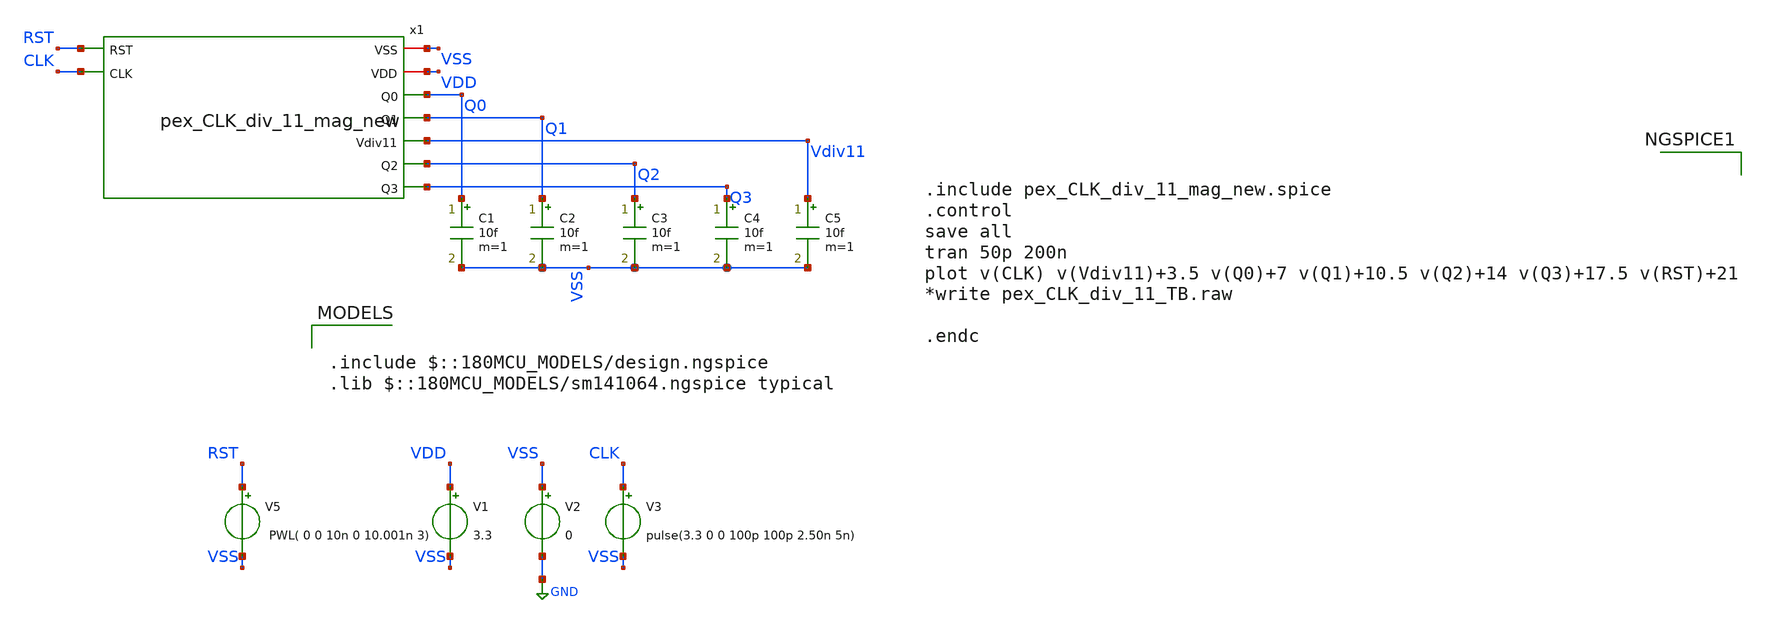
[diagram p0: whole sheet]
** sch_path: Clock_Generator_PAKISTAN_02/xschem/pex_CLK_div_11_TB.sch
**.subckt pex_CLK_div_11_TB
V1 VDD VSS 3.3
V2 VSS GND 0
V3 CLK VSS pulse(3.3 0 0 100p 100p 2.50n 5n)
C1 Q0 VSS 10f m=1
C2 Q1 VSS 10f m=1
C3 Q2 VSS 10f m=1
C4 Q3 VSS 10f m=1
C5 Vdiv11 VSS 10f m=1
V5 RST VSS PWL( 0 0 10n 0 10.001n 3)
x1 VSS VDD Q0 Q1 RST Vdiv11 Q2 Q3 CLK pex_CLK_div_11_mag_new
**** begin user architecture code

.include $::180MCU_MODELS/design.ngspice
.lib $::180MCU_MODELS/sm141064.ngspice typical



.include pex_CLK_div_11_mag_new.spice
.control
save all
tran 50p 200n
plot v(CLK) v(Vdiv11)+3.5 v(Q0)+7 v(Q1)+10.5 v(Q2)+14 v(Q3)+17.5 v(RST)+21
*write pex_CLK_div_11_TB.raw

.endc


**** end user architecture code
**.ends
.GLOBAL GND
.end
